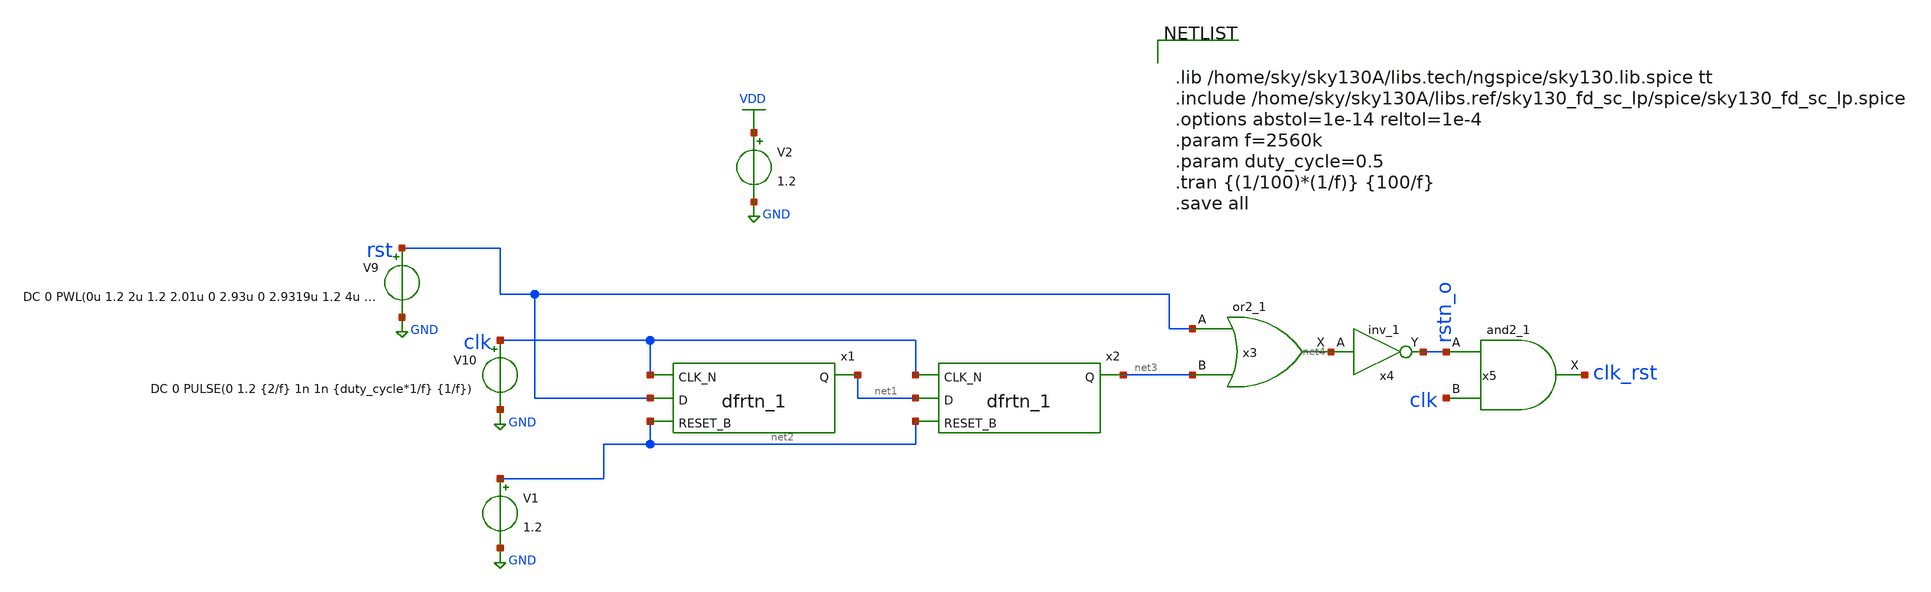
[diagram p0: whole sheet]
** sch_path: xschem/Clock Synchronizer/synchronizer.sch
**.subckt synchronizer
x1 clk rst net2 GND GND VDD VDD net1 sky130_fd_sc_lp__dfrtn_1
x3 rst net3 GND GND VDD VDD net4 sky130_fd_sc_lp__or2_1
x4 net4 GND GND VDD VDD rstn_o sky130_fd_sc_lp__inv_1
x2 clk net1 net2 GND GND VDD VDD net3 sky130_fd_sc_lp__dfrtn_1
V10 clk GND DC 0 PULSE(0 1.2 {2/f} 1n 1n {duty_cycle*1/f} {1/f})
V9 rst GND DC 0 PWL(0u 1.2 2u 1.2 2.01u 0 2.93u 0 2.9319u 1.2 4u 1.2 4.01u 0)
V2 VDD GND 1.2
V1 net2 GND 1.2
x5 rstn_o clk GND GND VDD VDD clk_rst sky130_fd_sc_lp__and2_1
**** begin user architecture code


.lib /home/sky/sky130A/libs.tech/ngspice/sky130.lib.spice tt
.include /home/sky/sky130A/libs.ref/sky130_fd_sc_lp/spice/sky130_fd_sc_lp.spice
.options abstol=1e-14 reltol=1e-4
.param f=2560k
.param duty_cycle=0.5
.tran {(1/100)*(1/f)} {100/f}
.save all


**** end user architecture code
**.ends
.GLOBAL GND
.GLOBAL VDD
.end
